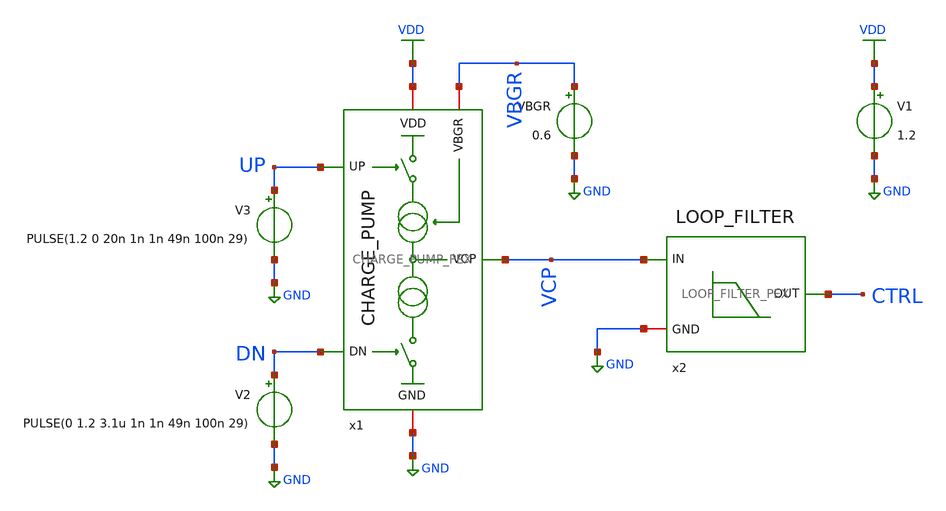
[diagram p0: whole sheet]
** sch_path: xschem/charge-pump/tb_CP_LF_PEX.sch
**.subckt tb_CP_LF_PEX
V1 VDD GND 1.2
V2 DN GND PULSE(0 1.2 3.1u 1n 1n 49n 100n 29)
V3 UP GND PULSE(1.2 0 20n 1n 1n 49n 100n 29)
VBGR VBGR GND 0.6
x1 UP VDD VCP VBGR GND DN CHARGE_PUMP_PEX
x2 CTRL VCP GND LOOP_FILTER_PEX
**** begin user architecture code



.include tb_CP.save
.param temp=27
.option method=gear rshunt=1.0e12
.control
save all
op
write tb_CP_LF.raw
.endc




.include /foss/designs/unicasss-tools/SG13G2_2.4GHz_LC_VCO_FPLL/pex/CHARGE_PUMP_V1__CHARGE_PUMP/magic_RC/CHARGE_PUMP.pex.spice
.include /foss/designs/unicasss-tools/SG13G2_2.4GHz_LC_VCO_FPLL/pex/LOOP_FILTER__LOOP_FILTER/magic_RC/LOOP_FILTER.pex.spice
.lib cornerMOSlv.lib mos_tt
.lib cornerMOShv.lib mos_tt
.lib cornerRES.lib res_typ
.lib cornerCAP.lib cap_typ




.param temp = 27
.options method=gear rshunt=1.0e12

.control

* Save required signals
save v(UP) v(DN) v(VCP) v(CTRL)

* Long transient simulation
tran 1n 6u

* Plot transient waveform
plot v(UP) v(DN) v(VCP) v(CTRL)
plot v(CTRL)

.endc



**** end user architecture code
**.ends
.GLOBAL VDD
.GLOBAL GND
.end
